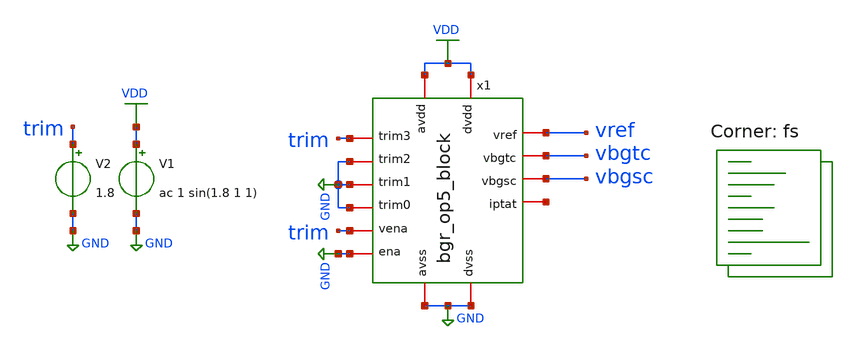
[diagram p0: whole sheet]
** sch_path: xschem/bgr_op5_block_tb_FS.sch
**.subckt bgr_op5_block_tb_FS
V1 VDD GND ac 1 sin(1.8 1 1)
V2 trim GND 1.8
x1 net1 VDD vbgtc GND trim vbgsc GND GND GND trim GND VDD GND vref bgr_op5_block
**** begin user architecture code


.include ~/chipalooza/sky130_gff_ip__bgr_1.2v/magic/bgr_op5_block_rev1.pex.spice
.option savecurrents
.control
save all
op
remzerovec
write bgr_op5_block_tb_FS.raw

set appendwrite
set wr_singlescale
set wr_vecnames
option numdgt=3

dc temp -40 85 1
remzerovec
*write bgr_op5_tb.raw
write VREF_FS.raw vref
*plot (ptat-ctat)
*plot ctat
plot vref
*wrdata vref5.csv vref
*plot vbgsc vbgtc

********TC********
meas dc temp_avg_vref avg v(vref)
meas dc temp_vref_27 find v(vref) when temp-sweep=27
meas dc temp_pp_vref PP v(vref)
meas dc temp_vref_max max v(vref)
meas dc temp_max_vref when v(vref)='temp_vref_max'
meas dc temp_vref_min min v(vref)
meas dc temp_min_vref when v(vref)='temp_vref_min'
let vref_tc='((temp_pp_vref*1000000)/(125*temp_avg_vref))'
print vref_tc

******PSRR******
ac dec 1000 1 10Meg
*write bgr_op5_tb.raw
write PSRR_FS.raw vdb(vref)
remzerovec
plot vdb(vref)
*wrdata PSRR5.csv vdb(vref)
meas ac psrr find vdb(vref) at=1k

****Power****
tran 10ms 500ms
*write bgr_op5_tb.raw
set altshow
show >> bgr_op5_block_tb_FS.lis
remzerovec
meas tran ave_v avg vdd
meas tran ave_i avg i(v1)
let ave_power='ave_v*(-ave_i)
plot vdd vref
plot vg1 vgstart start
*plot -i(v1)
print ave_power

*******LS******
dc v1 0 3.5 0.05
*write bgr_op5_tb.raw
remzerovec
plot vdd vref
meas dc vbg_27 find v(vref) at=1.8
meas dc vbgsc_27 find v(vbgsc) at=1.8
meas dc vbgtc_27 find v(vbgtc) at=1.8
meas dc vref_max max v(vref) from=1.62 to=1.98
meas dc vref_min min v(vref) from=1.62 to=1.98
let ls='(vref_max-vref_min)/(1.98-1.62)'
print ls

.endc


.lib $::SKYWATER_MODELS/sky130.lib.spice fs
**** end user architecture code
**.ends
.GLOBAL GND
.GLOBAL VDD
.end
